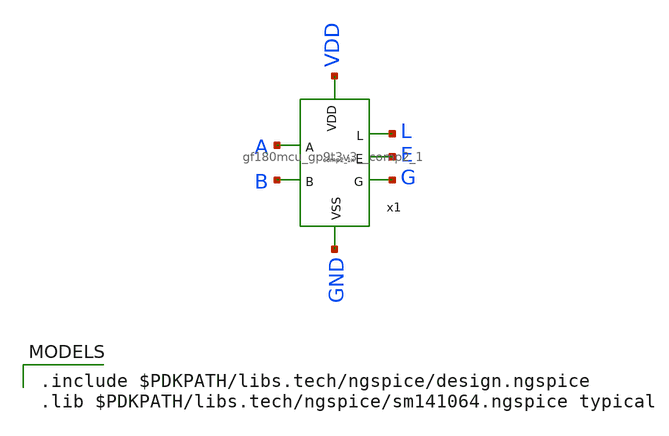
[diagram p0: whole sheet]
** sch_path: cells/comp2/schematics/testbench/tb_comp2_1x.sch
**.subckt tb_comp2_1x
x1 VDD L A E G B GND gf180mcu_gp9t3v3__comp2_1
**** begin user architecture code

.include $PDKPATH/libs.tech/ngspice/design.ngspice
.lib $PDKPATH/libs.tech/ngspice/sm141064.ngspice typical


* Stimuli
VPOWER VDD gnd DC 3.3
V_A A gnd PWL(0 0 {10n-10p} 0 {10n+10p} 3.3 {20n-10p} 3.3 {20n+10p} 0 {30n-10p} 0 {30n+10p} 3.3 40n 3.3)
V_B B gnd PWL(0 0 {20n-10p} 0 {20n+10p} 3.3 40n 3.3)

* Simulation
.tran 1p 40n
.control
run
save all
plot G E+4 L+8 B+12 A+16
.endc
.GLOBAL gnd
.end

**** end user architecture code
**.ends
.end
